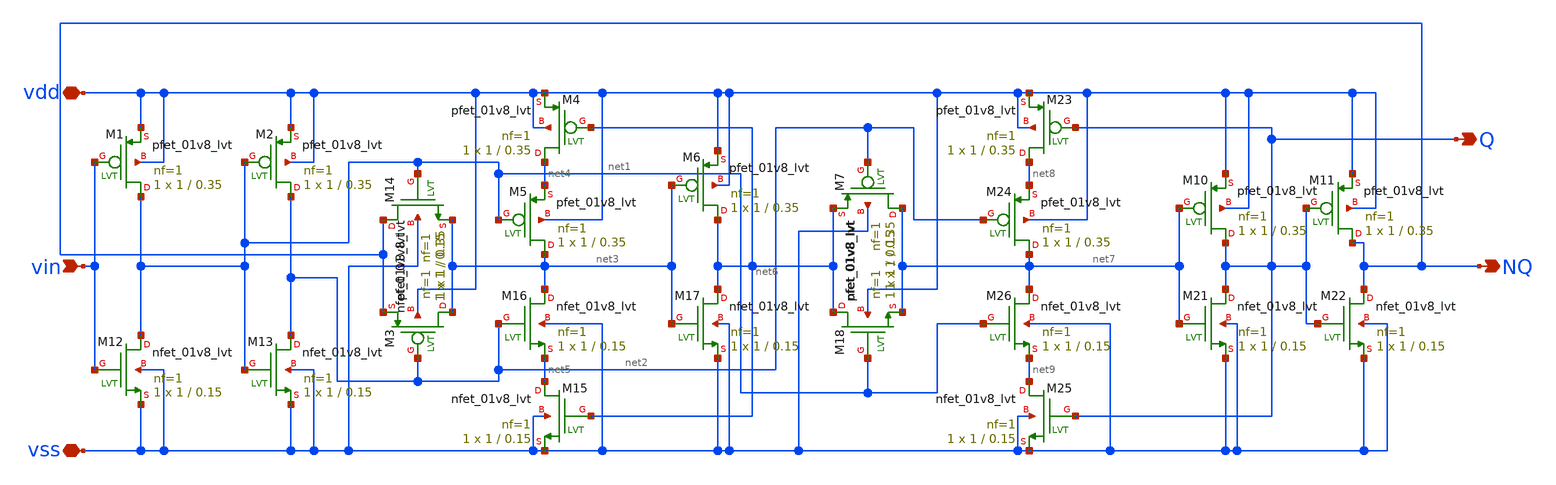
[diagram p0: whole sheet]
** sch_path: Circuits/lowpowersystem1/xschem/lowpowerdflipflop2sym.sch
**.subckt lowpowerdflipflop2sym Q NQ vdd vss vin
*.opin Q
*.opin NQ
*.iopin vdd
*.iopin vss
*.ipin vin
XM1 net1 vin vdd vdd sky130_fd_pr__pfet_01v8_lvt L=0.35 W=1 nf=1 ad='int((nf+1)/2) * W/nf * 0.29' as='int((nf+2)/2) * W/nf * 0.29'
+ pd='2*int((nf+1)/2) * (W/nf + 0.29)' ps='2*int((nf+2)/2) * (W/nf + 0.29)' nrd='0.29 / W' nrs='0.29 / W'
+ sa=0 sb=0 sd=0 mult=1 m=1
XM2 net2 net1 vdd vdd sky130_fd_pr__pfet_01v8_lvt L=0.35 W=1 nf=1 ad='int((nf+1)/2) * W/nf * 0.29' as='int((nf+2)/2) * W/nf * 0.29'
+ pd='2*int((nf+1)/2) * (W/nf + 0.29)' ps='2*int((nf+2)/2) * (W/nf + 0.29)' nrd='0.29 / W' nrs='0.29 / W'
+ sa=0 sb=0 sd=0 mult=1 m=1
XM3 net3 net2 NQ vdd sky130_fd_pr__pfet_01v8_lvt L=0.35 W=1 nf=1 ad='int((nf+1)/2) * W/nf * 0.29' as='int((nf+2)/2) * W/nf * 0.29'
+ pd='2*int((nf+1)/2) * (W/nf + 0.29)' ps='2*int((nf+2)/2) * (W/nf + 0.29)' nrd='0.29 / W' nrs='0.29 / W'
+ sa=0 sb=0 sd=0 mult=1 m=1
XM4 net4 net6 vdd vdd sky130_fd_pr__pfet_01v8_lvt L=0.35 W=1 nf=1 ad='int((nf+1)/2) * W/nf * 0.29' as='int((nf+2)/2) * W/nf * 0.29'
+ pd='2*int((nf+1)/2) * (W/nf + 0.29)' ps='2*int((nf+2)/2) * (W/nf + 0.29)' nrd='0.29 / W' nrs='0.29 / W'
+ sa=0 sb=0 sd=0 mult=1 m=1
XM5 net3 net1 net4 vdd sky130_fd_pr__pfet_01v8_lvt L=0.35 W=1 nf=1 ad='int((nf+1)/2) * W/nf * 0.29' as='int((nf+2)/2) * W/nf * 0.29'
+ pd='2*int((nf+1)/2) * (W/nf + 0.29)' ps='2*int((nf+2)/2) * (W/nf + 0.29)' nrd='0.29 / W' nrs='0.29 / W'
+ sa=0 sb=0 sd=0 mult=1 m=1
XM6 net6 net3 vdd vdd sky130_fd_pr__pfet_01v8_lvt L=0.35 W=1 nf=1 ad='int((nf+1)/2) * W/nf * 0.29' as='int((nf+2)/2) * W/nf * 0.29'
+ pd='2*int((nf+1)/2) * (W/nf + 0.29)' ps='2*int((nf+2)/2) * (W/nf + 0.29)' nrd='0.29 / W' nrs='0.29 / W'
+ sa=0 sb=0 sd=0 mult=1 m=1
XM7 net7 net2 net6 vss sky130_fd_pr__pfet_01v8_lvt L=0.35 W=1 nf=1 ad='int((nf+1)/2) * W/nf * 0.29' as='int((nf+2)/2) * W/nf * 0.29'
+ pd='2*int((nf+1)/2) * (W/nf + 0.29)' ps='2*int((nf+2)/2) * (W/nf + 0.29)' nrd='0.29 / W' nrs='0.29 / W'
+ sa=0 sb=0 sd=0 mult=1 m=1
XM10 Q net7 vdd vdd sky130_fd_pr__pfet_01v8_lvt L=0.35 W=1 nf=1 ad='int((nf+1)/2) * W/nf * 0.29' as='int((nf+2)/2) * W/nf * 0.29'
+ pd='2*int((nf+1)/2) * (W/nf + 0.29)' ps='2*int((nf+2)/2) * (W/nf + 0.29)' nrd='0.29 / W' nrs='0.29 / W'
+ sa=0 sb=0 sd=0 mult=1 m=1
XM11 NQ Q vdd vdd sky130_fd_pr__pfet_01v8_lvt L=0.35 W=1 nf=1 ad='int((nf+1)/2) * W/nf * 0.29' as='int((nf+2)/2) * W/nf * 0.29'
+ pd='2*int((nf+1)/2) * (W/nf + 0.29)' ps='2*int((nf+2)/2) * (W/nf + 0.29)' nrd='0.29 / W' nrs='0.29 / W'
+ sa=0 sb=0 sd=0 mult=1 m=1
XM12 net1 vin vss vss sky130_fd_pr__nfet_01v8_lvt L=0.15 W=1 nf=1 ad='int((nf+1)/2) * W/nf * 0.29' as='int((nf+2)/2) * W/nf * 0.29'
+ pd='2*int((nf+1)/2) * (W/nf + 0.29)' ps='2*int((nf+2)/2) * (W/nf + 0.29)' nrd='0.29 / W' nrs='0.29 / W'
+ sa=0 sb=0 sd=0 mult=1 m=1
XM13 net2 net1 vss vss sky130_fd_pr__nfet_01v8_lvt L=0.15 W=1 nf=1 ad='int((nf+1)/2) * W/nf * 0.29' as='int((nf+2)/2) * W/nf * 0.29'
+ pd='2*int((nf+1)/2) * (W/nf + 0.29)' ps='2*int((nf+2)/2) * (W/nf + 0.29)' nrd='0.29 / W' nrs='0.29 / W'
+ sa=0 sb=0 sd=0 mult=1 m=1
XM14 NQ net1 net3 vss sky130_fd_pr__nfet_01v8_lvt L=0.15 W=1 nf=1 ad='int((nf+1)/2) * W/nf * 0.29' as='int((nf+2)/2) * W/nf * 0.29'
+ pd='2*int((nf+1)/2) * (W/nf + 0.29)' ps='2*int((nf+2)/2) * (W/nf + 0.29)' nrd='0.29 / W' nrs='0.29 / W'
+ sa=0 sb=0 sd=0 mult=1 m=1
XM15 net5 net6 vss vss sky130_fd_pr__nfet_01v8_lvt L=0.15 W=1 nf=1 ad='int((nf+1)/2) * W/nf * 0.29' as='int((nf+2)/2) * W/nf * 0.29'
+ pd='2*int((nf+1)/2) * (W/nf + 0.29)' ps='2*int((nf+2)/2) * (W/nf + 0.29)' nrd='0.29 / W' nrs='0.29 / W'
+ sa=0 sb=0 sd=0 mult=1 m=1
XM16 net3 net2 net5 vss sky130_fd_pr__nfet_01v8_lvt L=0.15 W=1 nf=1 ad='int((nf+1)/2) * W/nf * 0.29'
+ as='int((nf+2)/2) * W/nf * 0.29' pd='2*int((nf+1)/2) * (W/nf + 0.29)' ps='2*int((nf+2)/2) * (W/nf + 0.29)'
+ nrd='0.29 / W' nrs='0.29 / W' sa=0 sb=0 sd=0 mult=1 m=1
XM17 net6 net3 vss vss sky130_fd_pr__nfet_01v8_lvt L=0.15 W=1 nf=1 ad='int((nf+1)/2) * W/nf * 0.29' as='int((nf+2)/2) * W/nf * 0.29'
+ pd='2*int((nf+1)/2) * (W/nf + 0.29)' ps='2*int((nf+2)/2) * (W/nf + 0.29)' nrd='0.29 / W' nrs='0.29 / W'
+ sa=0 sb=0 sd=0 mult=1 m=1
XM18 net6 net1 net7 vdd sky130_fd_pr__nfet_01v8_lvt L=0.15 W=1 nf=1 ad='int((nf+1)/2) * W/nf * 0.29'
+ as='int((nf+2)/2) * W/nf * 0.29' pd='2*int((nf+1)/2) * (W/nf + 0.29)' ps='2*int((nf+2)/2) * (W/nf + 0.29)'
+ nrd='0.29 / W' nrs='0.29 / W' sa=0 sb=0 sd=0 mult=1 m=1
XM21 Q net7 vss vss sky130_fd_pr__nfet_01v8_lvt L=0.15 W=1 nf=1 ad='int((nf+1)/2) * W/nf * 0.29' as='int((nf+2)/2) * W/nf * 0.29'
+ pd='2*int((nf+1)/2) * (W/nf + 0.29)' ps='2*int((nf+2)/2) * (W/nf + 0.29)' nrd='0.29 / W' nrs='0.29 / W'
+ sa=0 sb=0 sd=0 mult=1 m=1
XM22 NQ Q vss vss sky130_fd_pr__nfet_01v8_lvt L=0.15 W=1 nf=1 ad='int((nf+1)/2) * W/nf * 0.29' as='int((nf+2)/2) * W/nf * 0.29'
+ pd='2*int((nf+1)/2) * (W/nf + 0.29)' ps='2*int((nf+2)/2) * (W/nf + 0.29)' nrd='0.29 / W' nrs='0.29 / W'
+ sa=0 sb=0 sd=0 mult=1 m=1
XM23 net8 Q vdd vdd sky130_fd_pr__pfet_01v8_lvt L=0.35 W=1 nf=1 ad='int((nf+1)/2) * W/nf * 0.29' as='int((nf+2)/2) * W/nf * 0.29'
+ pd='2*int((nf+1)/2) * (W/nf + 0.29)' ps='2*int((nf+2)/2) * (W/nf + 0.29)' nrd='0.29 / W' nrs='0.29 / W'
+ sa=0 sb=0 sd=0 mult=1 m=1
XM24 net7 net2 net8 vdd sky130_fd_pr__pfet_01v8_lvt L=0.35 W=1 nf=1 ad='int((nf+1)/2) * W/nf * 0.29'
+ as='int((nf+2)/2) * W/nf * 0.29' pd='2*int((nf+1)/2) * (W/nf + 0.29)' ps='2*int((nf+2)/2) * (W/nf + 0.29)'
+ nrd='0.29 / W' nrs='0.29 / W' sa=0 sb=0 sd=0 mult=1 m=1
XM25 net9 Q vss vss sky130_fd_pr__nfet_01v8_lvt L=0.15 W=1 nf=1 ad='int((nf+1)/2) * W/nf * 0.29' as='int((nf+2)/2) * W/nf * 0.29'
+ pd='2*int((nf+1)/2) * (W/nf + 0.29)' ps='2*int((nf+2)/2) * (W/nf + 0.29)' nrd='0.29 / W' nrs='0.29 / W'
+ sa=0 sb=0 sd=0 mult=1 m=1
XM26 net7 net1 net9 vss sky130_fd_pr__nfet_01v8_lvt L=0.15 W=1 nf=1 ad='int((nf+1)/2) * W/nf * 0.29'
+ as='int((nf+2)/2) * W/nf * 0.29' pd='2*int((nf+1)/2) * (W/nf + 0.29)' ps='2*int((nf+2)/2) * (W/nf + 0.29)'
+ nrd='0.29 / W' nrs='0.29 / W' sa=0 sb=0 sd=0 mult=1 m=1
**.ends
.end
